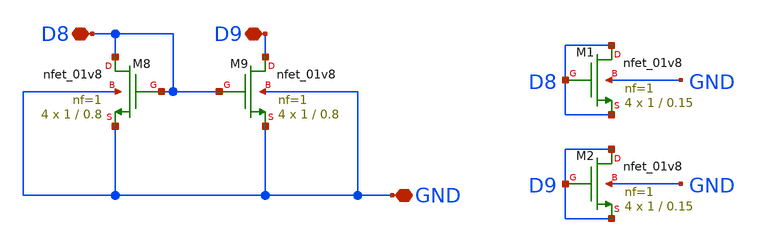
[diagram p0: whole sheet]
** sch_path: opamp/mag/nmoscs89.sch
**.subckt nmoscs89 GND D8 D9
*.iopin GND
*.iopin D8
*.iopin D9
XM8 D8 D8 GND GND sky130_fd_pr__nfet_01v8 L=0.8 W=1 nf=1 ad='int((nf+1)/2) * W/nf * 0.29' as='int((nf+2)/2) * W/nf * 0.29'
+ pd='2*int((nf+1)/2) * (W/nf + 0.29)' ps='2*int((nf+2)/2) * (W/nf + 0.29)' nrd='0.29 / W' nrs='0.29 / W'
+ sa=0 sb=0 sd=0 mult=4 m=4
XM9 D9 D8 GND GND sky130_fd_pr__nfet_01v8 L=0.8 W=1 nf=1 ad='int((nf+1)/2) * W/nf * 0.29' as='int((nf+2)/2) * W/nf * 0.29'
+ pd='2*int((nf+1)/2) * (W/nf + 0.29)' ps='2*int((nf+2)/2) * (W/nf + 0.29)' nrd='0.29 / W' nrs='0.29 / W'
+ sa=0 sb=0 sd=0 mult=4 m=4
XM1 D8 D8 D8 GND sky130_fd_pr__nfet_01v8 L=0.15 W=1 nf=1 ad='int((nf+1)/2) * W/nf * 0.29' as='int((nf+2)/2) * W/nf * 0.29'
+ pd='2*int((nf+1)/2) * (W/nf + 0.29)' ps='2*int((nf+2)/2) * (W/nf + 0.29)' nrd='0.29 / W' nrs='0.29 / W'
+ sa=0 sb=0 sd=0 mult=4 m=4
XM2 D9 D9 D9 GND sky130_fd_pr__nfet_01v8 L=0.15 W=1 nf=1 ad='int((nf+1)/2) * W/nf * 0.29' as='int((nf+2)/2) * W/nf * 0.29'
+ pd='2*int((nf+1)/2) * (W/nf + 0.29)' ps='2*int((nf+2)/2) * (W/nf + 0.29)' nrd='0.29 / W' nrs='0.29 / W'
+ sa=0 sb=0 sd=0 mult=4 m=4
**.ends
.end
